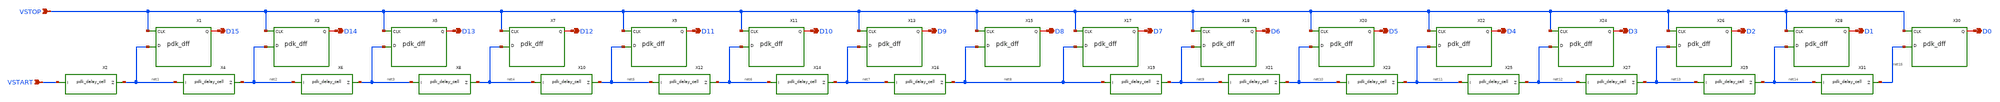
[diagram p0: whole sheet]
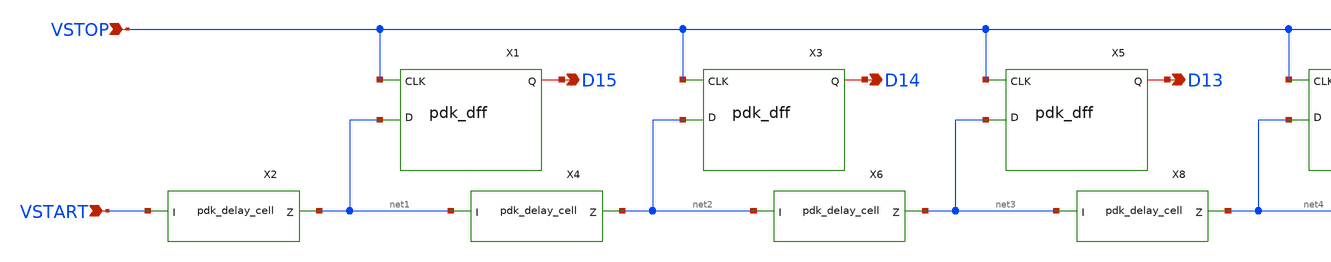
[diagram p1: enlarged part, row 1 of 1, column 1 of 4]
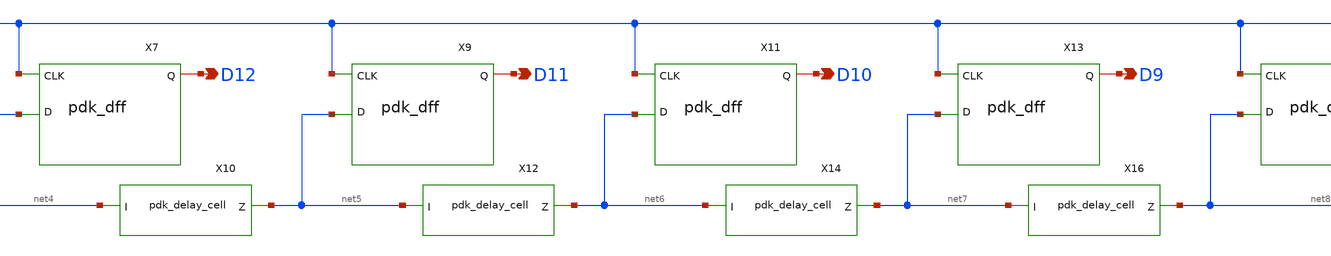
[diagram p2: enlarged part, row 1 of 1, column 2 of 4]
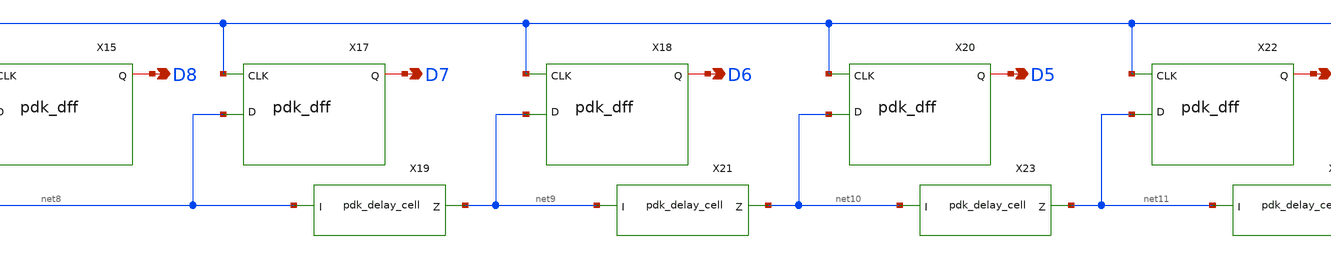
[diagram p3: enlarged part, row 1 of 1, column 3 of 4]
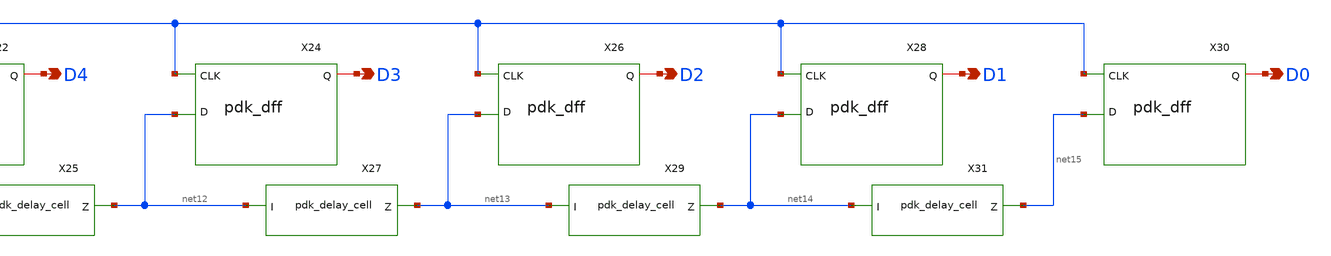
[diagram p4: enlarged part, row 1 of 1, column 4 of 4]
** sch_path: schem/medium_delay_line.sch
**.subckt medium_delay_line VSTOP VSTART D15 D14 D13 D12 D11 D10 D9 D8 D7 D6 D5 D4 D3 D2 D1 D0
*.ipin VSTOP
*.ipin VSTART
*.opin D15
*.opin D14
*.opin D13
*.opin D12
*.opin D11
*.opin D10
*.opin D9
*.opin D8
*.opin D7
*.opin D6
*.opin D5
*.opin D4
*.opin D3
*.opin D2
*.opin D1
*.opin D0
X1 net1 VSTOP D15 VDD VDD 0 0 gf180mcu_fd_sc_mcu7t5v0__dffq_4
X2 VSTART net1 VDD VDD 0 0 gf180mcu_fd_sc_mcu7t5v0__dlyc_1
X3 net2 VSTOP D14 VDD VDD 0 0 gf180mcu_fd_sc_mcu7t5v0__dffq_4
X4 net1 net2 VDD VDD 0 0 gf180mcu_fd_sc_mcu7t5v0__dlyc_1
X5 net3 VSTOP D13 VDD VDD 0 0 gf180mcu_fd_sc_mcu7t5v0__dffq_4
X6 net2 net3 VDD VDD 0 0 gf180mcu_fd_sc_mcu7t5v0__dlyc_1
X7 net4 VSTOP D12 VDD VDD 0 0 gf180mcu_fd_sc_mcu7t5v0__dffq_4
X8 net3 net4 VDD VDD 0 0 gf180mcu_fd_sc_mcu7t5v0__dlyc_1
X9 net5 VSTOP D11 VDD VDD 0 0 gf180mcu_fd_sc_mcu7t5v0__dffq_4
X10 net4 net5 VDD VDD 0 0 gf180mcu_fd_sc_mcu7t5v0__dlyc_1
X11 net6 VSTOP D10 VDD VDD 0 0 gf180mcu_fd_sc_mcu7t5v0__dffq_4
X12 net5 net6 VDD VDD 0 0 gf180mcu_fd_sc_mcu7t5v0__dlyc_1
X13 net7 VSTOP D9 VDD VDD 0 0 gf180mcu_fd_sc_mcu7t5v0__dffq_4
X14 net6 net7 VDD VDD 0 0 gf180mcu_fd_sc_mcu7t5v0__dlyc_1
X15 net8 VSTOP D8 VDD VDD 0 0 gf180mcu_fd_sc_mcu7t5v0__dffq_4
X16 net7 net8 VDD VDD 0 0 gf180mcu_fd_sc_mcu7t5v0__dlyc_1
X17 net8 VSTOP D7 VDD VDD 0 0 gf180mcu_fd_sc_mcu7t5v0__dffq_4
X18 net9 VSTOP D6 VDD VDD 0 0 gf180mcu_fd_sc_mcu7t5v0__dffq_4
X19 net8 net9 VDD VDD 0 0 gf180mcu_fd_sc_mcu7t5v0__dlyc_1
X20 net10 VSTOP D5 VDD VDD 0 0 gf180mcu_fd_sc_mcu7t5v0__dffq_4
X21 net9 net10 VDD VDD 0 0 gf180mcu_fd_sc_mcu7t5v0__dlyc_1
X22 net11 VSTOP D4 VDD VDD 0 0 gf180mcu_fd_sc_mcu7t5v0__dffq_4
X23 net10 net11 VDD VDD 0 0 gf180mcu_fd_sc_mcu7t5v0__dlyc_1
X24 net12 VSTOP D3 VDD VDD 0 0 gf180mcu_fd_sc_mcu7t5v0__dffq_4
X25 net11 net12 VDD VDD 0 0 gf180mcu_fd_sc_mcu7t5v0__dlyc_1
X26 net13 VSTOP D2 VDD VDD 0 0 gf180mcu_fd_sc_mcu7t5v0__dffq_4
X27 net12 net13 VDD VDD 0 0 gf180mcu_fd_sc_mcu7t5v0__dlyc_1
X28 net14 VSTOP D1 VDD VDD 0 0 gf180mcu_fd_sc_mcu7t5v0__dffq_4
X29 net13 net14 VDD VDD 0 0 gf180mcu_fd_sc_mcu7t5v0__dlyc_1
X30 net15 VSTOP D0 VDD VDD 0 0 gf180mcu_fd_sc_mcu7t5v0__dffq_4
X31 net14 net15 VDD VDD 0 0 gf180mcu_fd_sc_mcu7t5v0__dlyc_1
**.ends
.end
